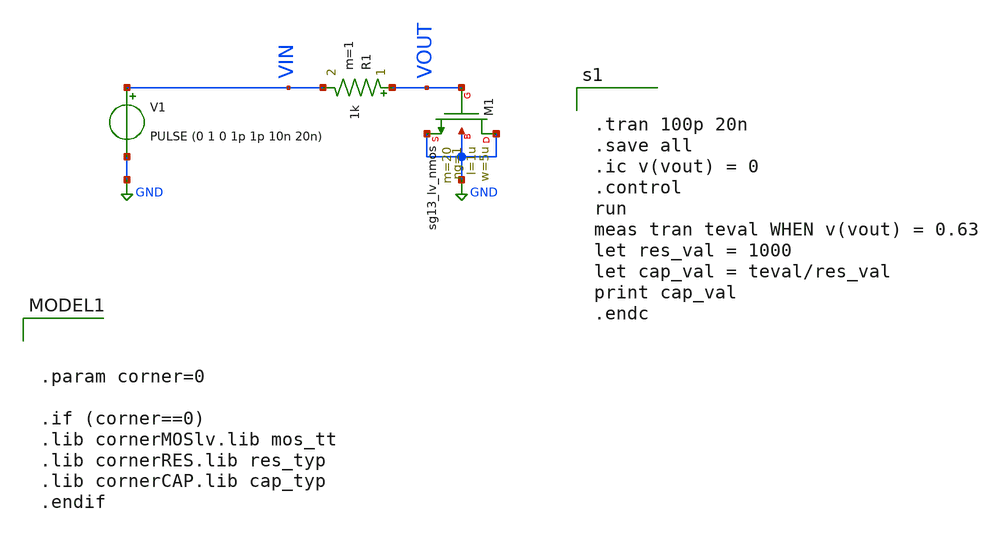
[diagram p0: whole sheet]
** sch_path: Day1/tb_cgate-ext_circuit.sch
**.subckt tb_cgate-ext_circuit
R1 VOUT VIN 1k m=1
V1 VIN GND PULSE (0 1 0 1p 1p 10n 20n)
XM1 GND VOUT GND GND sg13_lv_nmos w=5u l=1u ng=1 m=20 mm_ok=1
**** begin user architecture code


.tran 100p 20n
.save all
.ic v(vout) = 0
.control
run
meas tran teval WHEN v(vout) = 0.63
let res_val = 1000
let cap_val = teval/res_val
print cap_val
.endc




.param corner=0

.if (corner==0)
.lib cornerMOSlv.lib mos_tt
.lib cornerRES.lib res_typ
.lib cornerCAP.lib cap_typ
.endif

**** end user architecture code
**.ends
.GLOBAL GND
.end
